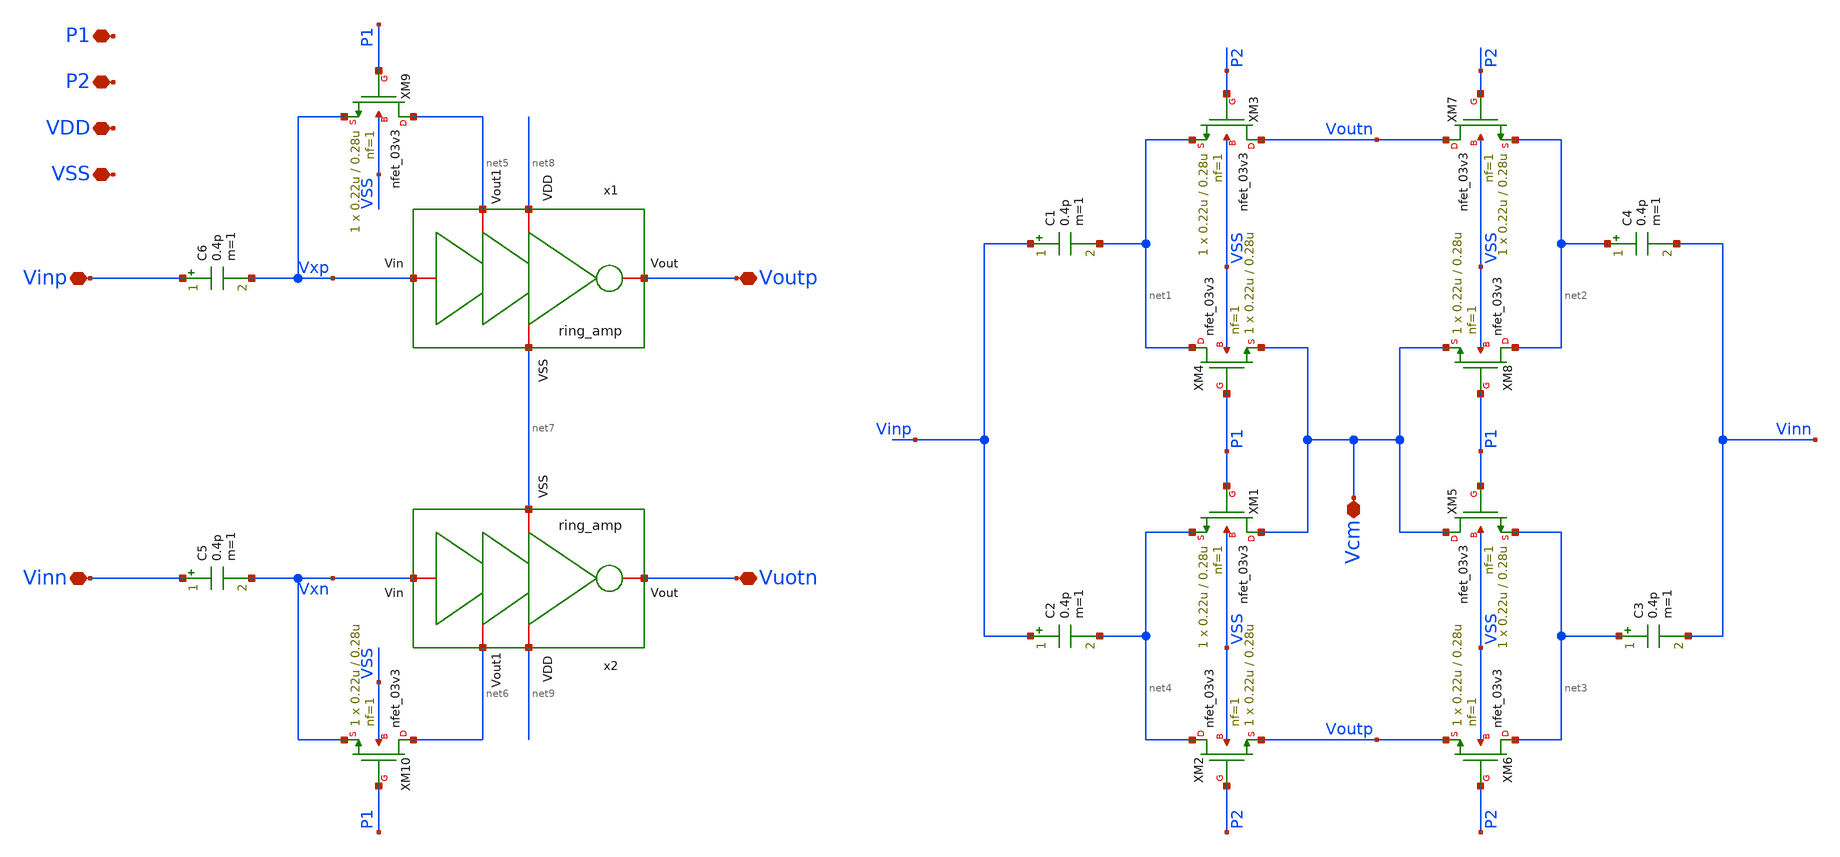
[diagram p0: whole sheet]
** sch_path: designs/DS_modulator/ring_amp_diff/xschem/ring_amp_diff.sch
**.subckt ring_amp_diff P1 P2 VDD VSS Vcm Vinp Vinn Voutp Vuotn
*.iopin P1
*.iopin P2
*.iopin VDD
*.iopin VSS
*.iopin Vcm
*.iopin Vinp
*.iopin Vinn
*.iopin Voutp
*.iopin Vuotn
x1 net8 Vxp Voutp net5 net7 ring_amp
x2 net9 Vxn Vuotn net6 net7 ring_amp
XM1 Vcm P1 net4 VSS nfet_03v3 L=0.28u W=0.22u nf=1 ad='int((nf+1)/2) * W/nf * 0.18u' as='int((nf+2)/2) * W/nf * 0.18u'
+ pd='2*int((nf+1)/2) * (W/nf + 0.18u)' ps='2*int((nf+2)/2) * (W/nf + 0.18u)' nrd='0.18u / W' nrs='0.18u / W'
+ sa=0 sb=0 sd=0 m=1
XM2 net4 P2 Voutp VSS nfet_03v3 L=0.28u W=0.22u nf=1 ad='int((nf+1)/2) * W/nf * 0.18u' as='int((nf+2)/2) * W/nf * 0.18u'
+ pd='2*int((nf+1)/2) * (W/nf + 0.18u)' ps='2*int((nf+2)/2) * (W/nf + 0.18u)' nrd='0.18u / W' nrs='0.18u / W'
+ sa=0 sb=0 sd=0 m=1
XM3 Voutn P2 net1 VSS nfet_03v3 L=0.28u W=0.22u nf=1 ad='int((nf+1)/2) * W/nf * 0.18u' as='int((nf+2)/2) * W/nf * 0.18u'
+ pd='2*int((nf+1)/2) * (W/nf + 0.18u)' ps='2*int((nf+2)/2) * (W/nf + 0.18u)' nrd='0.18u / W' nrs='0.18u / W'
+ sa=0 sb=0 sd=0 m=1
XM4 net1 P1 Vcm VSS nfet_03v3 L=0.28u W=0.22u nf=1 ad='int((nf+1)/2) * W/nf * 0.18u' as='int((nf+2)/2) * W/nf * 0.18u'
+ pd='2*int((nf+1)/2) * (W/nf + 0.18u)' ps='2*int((nf+2)/2) * (W/nf + 0.18u)' nrd='0.18u / W' nrs='0.18u / W'
+ sa=0 sb=0 sd=0 m=1
XM5 Vcm P1 net3 VSS nfet_03v3 L=0.28u W=0.22u nf=1 ad='int((nf+1)/2) * W/nf * 0.18u' as='int((nf+2)/2) * W/nf * 0.18u'
+ pd='2*int((nf+1)/2) * (W/nf + 0.18u)' ps='2*int((nf+2)/2) * (W/nf + 0.18u)' nrd='0.18u / W' nrs='0.18u / W'
+ sa=0 sb=0 sd=0 m=1
XM6 net3 P2 Voutp VSS nfet_03v3 L=0.28u W=0.22u nf=1 ad='int((nf+1)/2) * W/nf * 0.18u' as='int((nf+2)/2) * W/nf * 0.18u'
+ pd='2*int((nf+1)/2) * (W/nf + 0.18u)' ps='2*int((nf+2)/2) * (W/nf + 0.18u)' nrd='0.18u / W' nrs='0.18u / W'
+ sa=0 sb=0 sd=0 m=1
XM7 Voutn P2 net2 VSS nfet_03v3 L=0.28u W=0.22u nf=1 ad='int((nf+1)/2) * W/nf * 0.18u' as='int((nf+2)/2) * W/nf * 0.18u'
+ pd='2*int((nf+1)/2) * (W/nf + 0.18u)' ps='2*int((nf+2)/2) * (W/nf + 0.18u)' nrd='0.18u / W' nrs='0.18u / W'
+ sa=0 sb=0 sd=0 m=1
XM8 net2 P1 Vcm VSS nfet_03v3 L=0.28u W=0.22u nf=1 ad='int((nf+1)/2) * W/nf * 0.18u' as='int((nf+2)/2) * W/nf * 0.18u'
+ pd='2*int((nf+1)/2) * (W/nf + 0.18u)' ps='2*int((nf+2)/2) * (W/nf + 0.18u)' nrd='0.18u / W' nrs='0.18u / W'
+ sa=0 sb=0 sd=0 m=1
XM9 net5 P1 Vxp VSS nfet_03v3 L=0.28u W=0.22u nf=1 ad='int((nf+1)/2) * W/nf * 0.18u' as='int((nf+2)/2) * W/nf * 0.18u'
+ pd='2*int((nf+1)/2) * (W/nf + 0.18u)' ps='2*int((nf+2)/2) * (W/nf + 0.18u)' nrd='0.18u / W' nrs='0.18u / W'
+ sa=0 sb=0 sd=0 m=1
XM10 net6 P1 Vxn VSS nfet_03v3 L=0.28u W=0.22u nf=1 ad='int((nf+1)/2) * W/nf * 0.18u' as='int((nf+2)/2) * W/nf * 0.18u'
+ pd='2*int((nf+1)/2) * (W/nf + 0.18u)' ps='2*int((nf+2)/2) * (W/nf + 0.18u)' nrd='0.18u / W' nrs='0.18u / W'
+ sa=0 sb=0 sd=0 m=1
C1 Vinp net1 0.4p m=1
C2 Vinp net4 0.4p m=1
C3 net3 Vinn 0.4p m=1
C4 net2 Vinn 0.4p m=1
C5 Vinn Vxn 0.4p m=1
C6 Vinp Vxp 0.4p m=1
**.ends
.end
